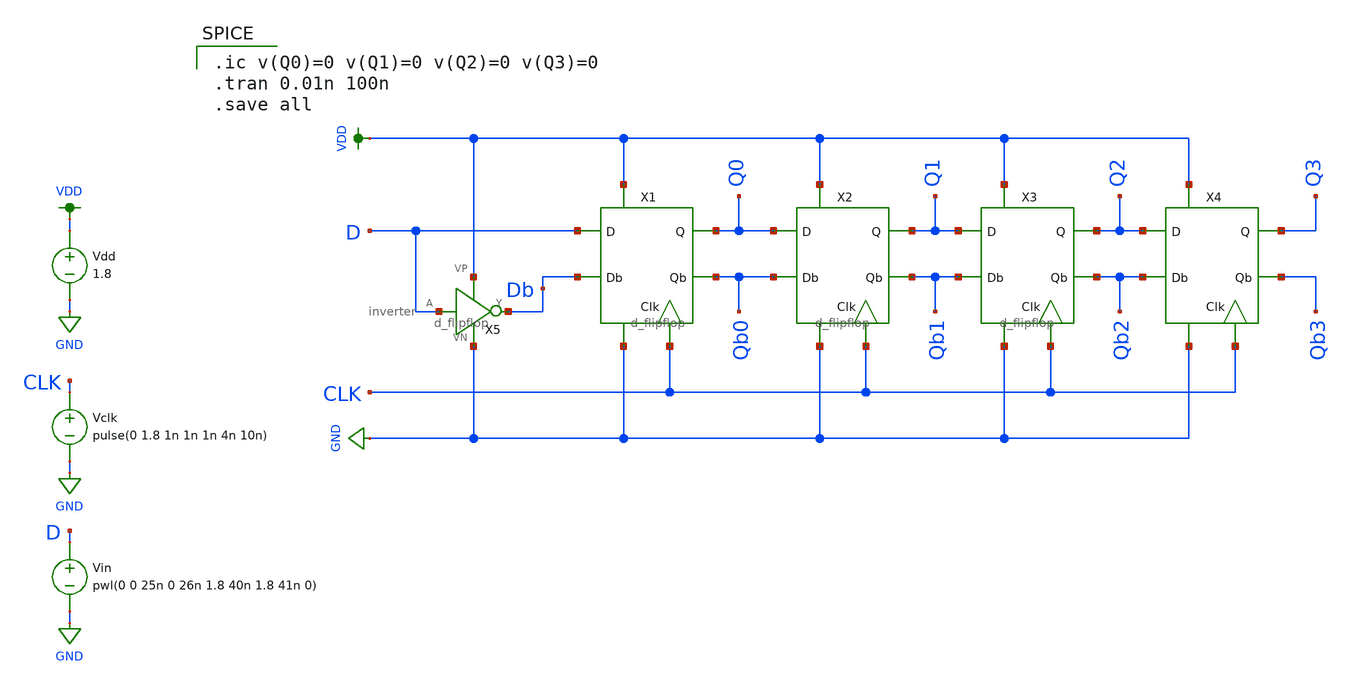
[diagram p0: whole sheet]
** sch_path: mp2/sreg/sreg_test_harness.sch
**.subckt sreg_test_harness
X1 D Db CLK Qb0 Q0 GND VDD d_flipflop
X2 Q0 Qb0 CLK Qb1 Q1 GND VDD d_flipflop
X3 Q1 Qb1 CLK Qb2 Q2 GND VDD d_flipflop
X4 Q2 Qb2 CLK Qb3 Q3 GND VDD d_flipflop
X5 D Db VDD GND inverter
Vdd VDD GND 1.8
Vclk CLK GND pulse(0 1.8 1n 1n 1n 4n 10n)
Vin D GND pwl(0 0 25n 0 26n 1.8 40n 1.8 41n 0)
**** begin user architecture code

.option wnflag=1
.lib ~/skywater/skywater-pdk/libraries/sky130_fd_pr_ngspice/latest/models/sky130.lib.spice tt


.ic v(Q0)=0 v(Q1)=0 v(Q2)=0 v(Q3)=0
.tran 0.01n 100n
.save all

**** end user architecture code
**.ends

* expanding   symbol:  /home/madvlsi/Documents/mp2/d_flipflop/d_flipflop.sym # of pins=7
** sym_path: mp2/d_flipflop/d_flipflop.sym
** sch_path: mp2/d_flipflop/d_flipflop.sch
.subckt d_flipflop D Db CLK Qb Q VN VP
*.ipin D
*.ipin CLK
*.opin Q
*.opin Qb
*.ipin Db
*.iopin VP
*.iopin VN
XM1 D CLK net2 VP sky130_fd_pr__pfet_01v8 L=0.15 W=1 nf=1 ad='int((nf+1)/2) * W/nf * 0.29' as='int((nf+2)/2) * W/nf * 0.29'
+ pd='2*int((nf+1)/2) * (W/nf + 0.29)' ps='2*int((nf+2)/2) * (W/nf + 0.29)' nrd='0.29 / W' nrs='0.29 / W'
+ sa=0 sb=0 sd=0 mult=1 m=1
XM2 Db CLK net3 VP sky130_fd_pr__pfet_01v8 L=0.15 W=1 nf=1 ad='int((nf+1)/2) * W/nf * 0.29' as='int((nf+2)/2) * W/nf * 0.29'
+ pd='2*int((nf+1)/2) * (W/nf + 0.29)' ps='2*int((nf+2)/2) * (W/nf + 0.29)' nrd='0.29 / W' nrs='0.29 / W'
+ sa=0 sb=0 sd=0 mult=1 m=1
XM3 VP net2 net3 VP sky130_fd_pr__pfet_01v8 L=0.15 W=1 nf=1 ad='int((nf+1)/2) * W/nf * 0.29' as='int((nf+2)/2) * W/nf * 0.29'
+ pd='2*int((nf+1)/2) * (W/nf + 0.29)' ps='2*int((nf+2)/2) * (W/nf + 0.29)' nrd='0.29 / W' nrs='0.29 / W'
+ sa=0 sb=0 sd=0 mult=1 m=1
XM5 net3 net2 net1 VN sky130_fd_pr__nfet_01v8 L=0.15 W=1 nf=1 ad='int((nf+1)/2) * W/nf * 0.29' as='int((nf+2)/2) * W/nf * 0.29'
+ pd='2*int((nf+1)/2) * (W/nf + 0.29)' ps='2*int((nf+2)/2) * (W/nf + 0.29)' nrd='0.29 / W' nrs='0.29 / W'
+ sa=0 sb=0 sd=0 mult=1 m=1
XM7 net1 CLK VN VN sky130_fd_pr__nfet_01v8 L=0.15 W=4 nf=1 ad='int((nf+1)/2) * W/nf * 0.29' as='int((nf+2)/2) * W/nf * 0.29'
+ pd='2*int((nf+1)/2) * (W/nf + 0.29)' ps='2*int((nf+2)/2) * (W/nf + 0.29)' nrd='0.29 / W' nrs='0.29 / W'
+ sa=0 sb=0 sd=0 mult=1 m=1
XM8 Q CLK net2 VN sky130_fd_pr__nfet_01v8 L=0.15 W=1 nf=1 ad='int((nf+1)/2) * W/nf * 0.29' as='int((nf+2)/2) * W/nf * 0.29'
+ pd='2*int((nf+1)/2) * (W/nf + 0.29)' ps='2*int((nf+2)/2) * (W/nf + 0.29)' nrd='0.29 / W' nrs='0.29 / W'
+ sa=0 sb=0 sd=0 mult=1 m=1
XM9 Qb CLK net3 VN sky130_fd_pr__nfet_01v8 L=0.15 W=1 nf=1 ad='int((nf+1)/2) * W/nf * 0.29' as='int((nf+2)/2) * W/nf * 0.29'
+ pd='2*int((nf+1)/2) * (W/nf + 0.29)' ps='2*int((nf+2)/2) * (W/nf + 0.29)' nrd='0.29 / W' nrs='0.29 / W'
+ sa=0 sb=0 sd=0 mult=1 m=1
XM10 net4 Q Qb VP sky130_fd_pr__pfet_01v8 L=0.15 W=1 nf=1 ad='int((nf+1)/2) * W/nf * 0.29' as='int((nf+2)/2) * W/nf * 0.29'
+ pd='2*int((nf+1)/2) * (W/nf + 0.29)' ps='2*int((nf+2)/2) * (W/nf + 0.29)' nrd='0.29 / W' nrs='0.29 / W'
+ sa=0 sb=0 sd=0 mult=1 m=1
XM11 net4 Qb Q VP sky130_fd_pr__pfet_01v8 L=0.15 W=1 nf=1 ad='int((nf+1)/2) * W/nf * 0.29' as='int((nf+2)/2) * W/nf * 0.29'
+ pd='2*int((nf+1)/2) * (W/nf + 0.29)' ps='2*int((nf+2)/2) * (W/nf + 0.29)' nrd='0.29 / W' nrs='0.29 / W'
+ sa=0 sb=0 sd=0 mult=1 m=1
XM12 VP CLK net4 VP sky130_fd_pr__pfet_01v8 L=0.15 W=4 nf=1 ad='int((nf+1)/2) * W/nf * 0.29' as='int((nf+2)/2) * W/nf * 0.29'
+ pd='2*int((nf+1)/2) * (W/nf + 0.29)' ps='2*int((nf+2)/2) * (W/nf + 0.29)' nrd='0.29 / W' nrs='0.29 / W'
+ sa=0 sb=0 sd=0 mult=1 m=1
XM13 Qb Q VN VN sky130_fd_pr__nfet_01v8 L=0.15 W=1 nf=1 ad='int((nf+1)/2) * W/nf * 0.29' as='int((nf+2)/2) * W/nf * 0.29'
+ pd='2*int((nf+1)/2) * (W/nf + 0.29)' ps='2*int((nf+2)/2) * (W/nf + 0.29)' nrd='0.29 / W' nrs='0.29 / W'
+ sa=0 sb=0 sd=0 mult=1 m=1
XM14 Q Qb VN VN sky130_fd_pr__nfet_01v8 L=0.15 W=1 nf=1 ad='int((nf+1)/2) * W/nf * 0.29' as='int((nf+2)/2) * W/nf * 0.29'
+ pd='2*int((nf+1)/2) * (W/nf + 0.29)' ps='2*int((nf+2)/2) * (W/nf + 0.29)' nrd='0.29 / W' nrs='0.29 / W'
+ sa=0 sb=0 sd=0 mult=1 m=1
XM4 VP net3 net2 VP sky130_fd_pr__pfet_01v8 L=0.15 W=1 nf=1 ad='int((nf+1)/2) * W/nf * 0.29' as='int((nf+2)/2) * W/nf * 0.29'
+ pd='2*int((nf+1)/2) * (W/nf + 0.29)' ps='2*int((nf+2)/2) * (W/nf + 0.29)' nrd='0.29 / W' nrs='0.29 / W'
+ sa=0 sb=0 sd=0 mult=1 m=1
XM6 net2 net3 net1 VN sky130_fd_pr__nfet_01v8 L=0.15 W=1 nf=1 ad='int((nf+1)/2) * W/nf * 0.29' as='int((nf+2)/2) * W/nf * 0.29'
+ pd='2*int((nf+1)/2) * (W/nf + 0.29)' ps='2*int((nf+2)/2) * (W/nf + 0.29)' nrd='0.29 / W' nrs='0.29 / W'
+ sa=0 sb=0 sd=0 mult=1 m=1
.ends


* expanding   symbol:  /home/madvlsi/Documents/mp1/inverter/inverter.sym # of pins=4
** sym_path: mp1/inverter/inverter.sym
** sch_path: mp1/inverter/inverter.sch
.subckt inverter A Y VP VN
*.ipin A
*.iopin VP
*.iopin VN
*.opin Y
XM1 Y A VN VN sky130_fd_pr__nfet_01v8 L=0.15 W=1 nf=1 ad='int((nf+1)/2) * W/nf * 0.29' as='int((nf+2)/2) * W/nf * 0.29'
+ pd='2*int((nf+1)/2) * (W/nf + 0.29)' ps='2*int((nf+2)/2) * (W/nf + 0.29)' nrd='0.29 / W' nrs='0.29 / W'
+ sa=0 sb=0 sd=0 mult=1 m=1
XM2 Y A VP VP sky130_fd_pr__pfet_01v8 L=0.15 W=1 nf=1 ad='int((nf+1)/2) * W/nf * 0.29' as='int((nf+2)/2) * W/nf * 0.29'
+ pd='2*int((nf+1)/2) * (W/nf + 0.29)' ps='2*int((nf+2)/2) * (W/nf + 0.29)' nrd='0.29 / W' nrs='0.29 / W'
+ sa=0 sb=0 sd=0 mult=1 m=1
.ends

.GLOBAL VDD
.GLOBAL GND
.end
